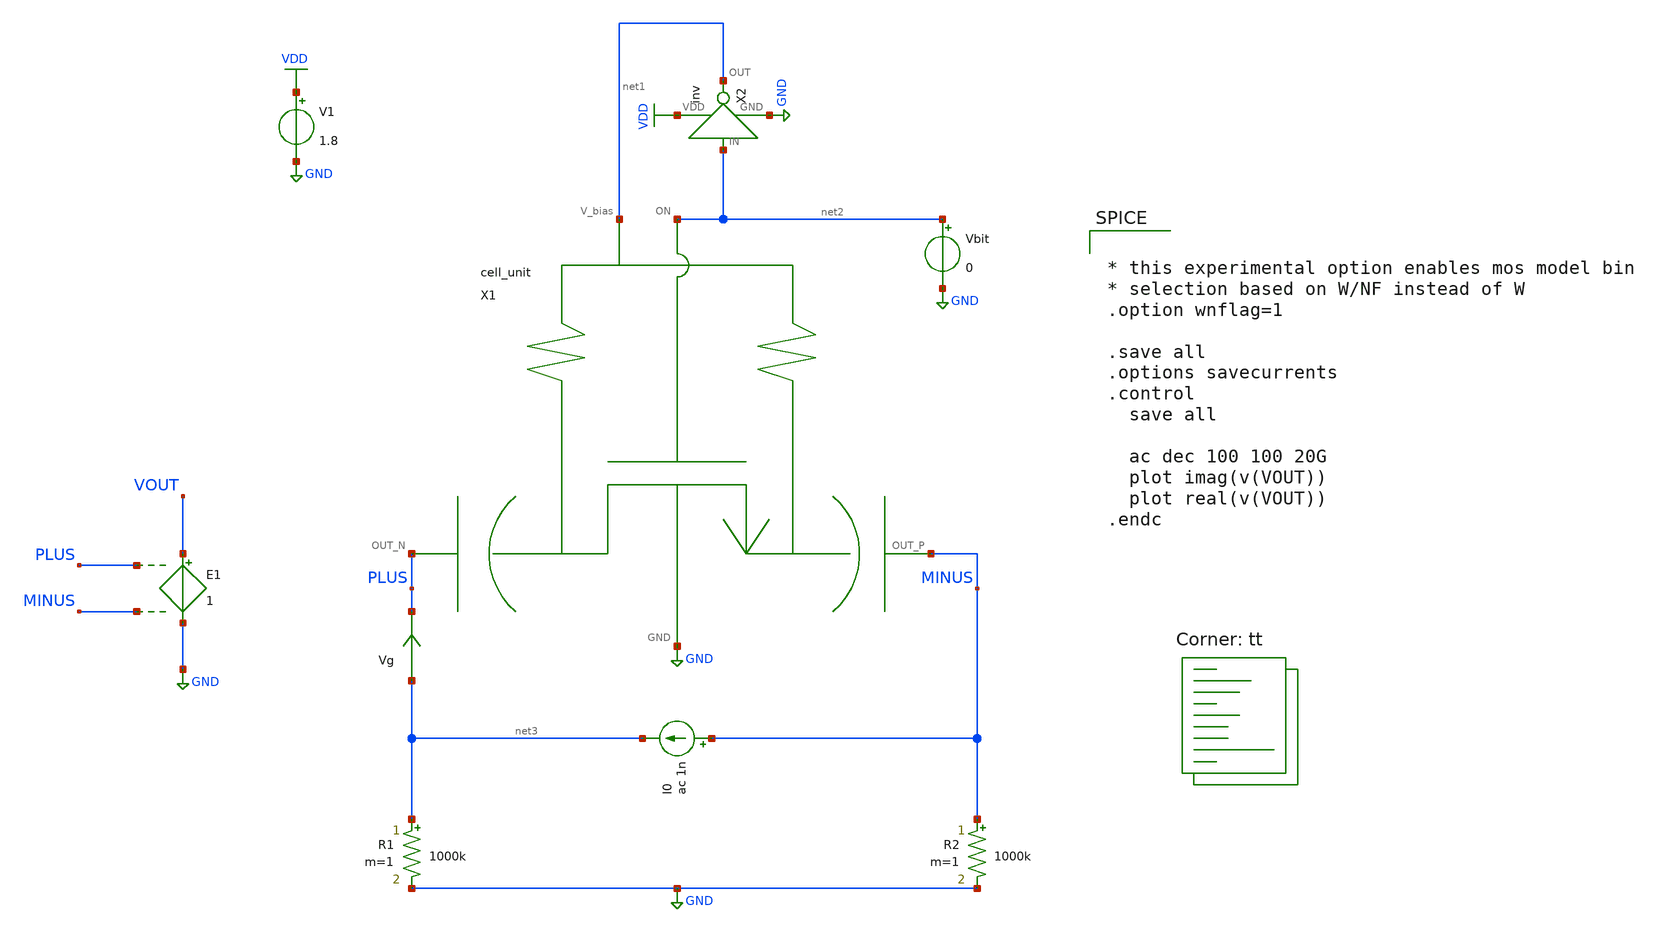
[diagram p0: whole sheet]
** sch_path: xschem/cell_unit_tb.sch
**.subckt cell_unit_tb
V1 VDD GND 1.8
X1 net1 net2 PLUS GND MINUS cell_unit
Vbit net2 GND 0
X2 net2 net1 VDD GND inv
R1 net3 GND 1000k m=1
R2 MINUS GND 1000k m=1
Vg net3 PLUS 0
.save i(vg)
E1 VOUT GND PLUS MINUS 1
I0 MINUS net3 ac 1n
**** begin user architecture code


* this experimental option enables mos model bin
* selection based on W/NF instead of W
.option wnflag=1

.save all
.options savecurrents
.control
  save all

  ac dec 100 100 20G
  plot imag(v(VOUT))
  plot real(v(VOUT))
.endc



.lib $::SKYWATER_MODELS/sky130.lib.spice tt
**** end user architecture code
**.ends

* expanding   symbol:  cell_unit.sym # of pins=5
** sym_path: xschem/cell_unit.sym
** sch_path: xschem/cell_unit.sch
.subckt cell_unit V_bias ON OUT_N GND OUT_P
*.iopin OUT_N
*.iopin OUT_P
*.iopin GND
*.ipin ON
*.ipin V_bias
XC1 OUT_N net1 sky130_fd_pr__cap_mim_m3_1 W=3.3 L=3.3 MF=1 m=1
XC2 OUT_P net2 sky130_fd_pr__cap_mim_m3_1 W=3.3 L=3.3 MF=1 m=1
XR1 net1 V_bias GND sky130_fd_pr__res_xhigh_po_0p35 L=1.5 mult=1 m=1
XR2 net2 V_bias GND sky130_fd_pr__res_xhigh_po_0p35 L=1.5 mult=1 m=1
X1 sky130_fd_pr__rf_nfet_01v8_aM02W1p65L0p15 net2 ON net1 GND
.ends


* expanding   symbol:  inv.sym # of pins=4
** sym_path: xschem/inv.sym
** sch_path: xschem/inv.sch
.subckt inv IN OUT VDD GND
*.ipin IN
*.opin OUT
*.iopin VDD
*.iopin GND
XM1 OUT IN GND GND sky130_fd_pr__nfet_01v8 L=0.15 W=1.5 nf=1 ad='int((nf+1)/2) * W/nf * 0.29' as='int((nf+2)/2) * W/nf * 0.29'
+ pd='2*int((nf+1)/2) * (W/nf + 0.29)' ps='2*int((nf+2)/2) * (W/nf + 0.29)' nrd='0.29 / W' nrs='0.29 / W'
+ sa=0 sb=0 sd=0 mult=1 m=1
XM2 OUT IN VDD VDD sky130_fd_pr__pfet_01v8 L=0.15 W=3 nf=1 ad='int((nf+1)/2) * W/nf * 0.29' as='int((nf+2)/2) * W/nf * 0.29'
+ pd='2*int((nf+1)/2) * (W/nf + 0.29)' ps='2*int((nf+2)/2) * (W/nf + 0.29)' nrd='0.29 / W' nrs='0.29 / W'
+ sa=0 sb=0 sd=0 mult=1 m=1
.ends


* expanding   symbol:  sky130_fd_pr__rf_nfet_01v8_aM02W1p65L0p15.sym # of pins=4
** sym_path: xschem/sky130_fd_pr__rf_nfet_01v8_aM02W1p65L0p15.sym
** sch_path: xschem/sky130_fd_pr__rf_nfet_01v8_aM02W1p65L0p15.sch
.subckt sky130_fd_pr__rf_nfet_01v8_aM02W1p65L0p15
*.iopin SOURCE
*.iopin DRAIN
*.ipin SUBSTRATE
*.ipin GATE
**** begin user architecture code


.subckt sky130_fd_pr__rf_nfet_01v8_aM02W1p65L0p15 DRAIN GATE SOURCE SUBSTRATE
X0 SOURCE GATE DRAIN SUBSTRATE sky130_fd_pr__nfet_01v8 w=1.65e+06u l=150000u
X1 DRAIN GATE SOURCE SUBSTRATE sky130_fd_pr__nfet_01v8 w=1.65e+06u l=150000u
.ends

**** end user architecture code
.ends

.GLOBAL GND
.GLOBAL VDD
.end
